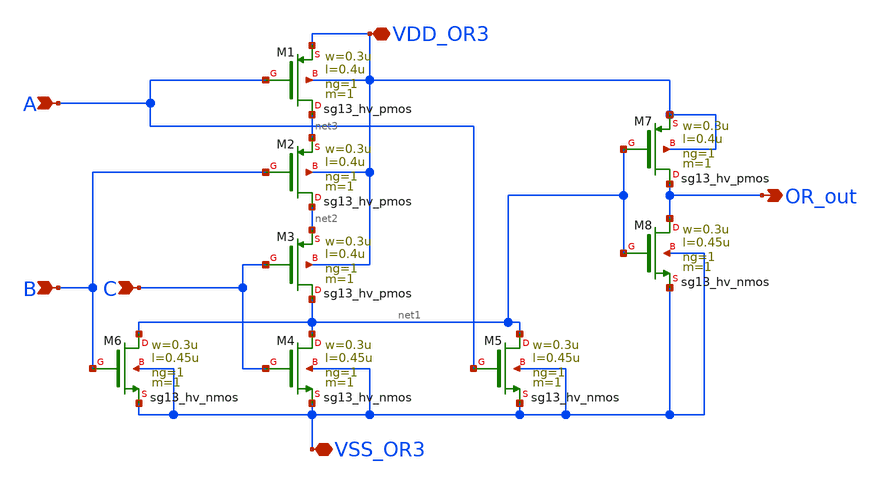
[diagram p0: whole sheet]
** sch_path: circuit_files/sarADC/or3.sch
**.subckt or3 VDD_OR3 VSS_OR3 OR_out A B C
*.iopin VDD_OR3
*.iopin VSS_OR3
*.opin OR_out
*.ipin A
*.ipin B
*.ipin C
XM1 net3 A VDD_OR3 VDD_OR3 sg13_hv_pmos w=0.3u l=0.4u ng=1 m=1 mm_ok=1
XM2 net2 B net3 VDD_OR3 sg13_hv_pmos w=0.3u l=0.4u ng=1 m=1 mm_ok=1
XM3 net1 C net2 VDD_OR3 sg13_hv_pmos w=0.3u l=0.4u ng=1 m=1 mm_ok=1
XM4 net1 C VSS_OR3 VSS_OR3 sg13_hv_nmos w=0.3u l=0.45u ng=1 m=1 mm_ok=1
XM5 net1 A VSS_OR3 VSS_OR3 sg13_hv_nmos w=0.3u l=0.45u ng=1 m=1 mm_ok=1
XM6 net1 B VSS_OR3 VSS_OR3 sg13_hv_nmos w=0.3u l=0.45u ng=1 m=1 mm_ok=1
XM7 OR_out net1 VDD_OR3 VDD_OR3 sg13_hv_pmos w=0.3u l=0.4u ng=1 m=1 mm_ok=1
XM8 OR_out net1 VSS_OR3 VSS_OR3 sg13_hv_nmos w=0.3u l=0.45u ng=1 m=1 mm_ok=1
**.ends
.end
